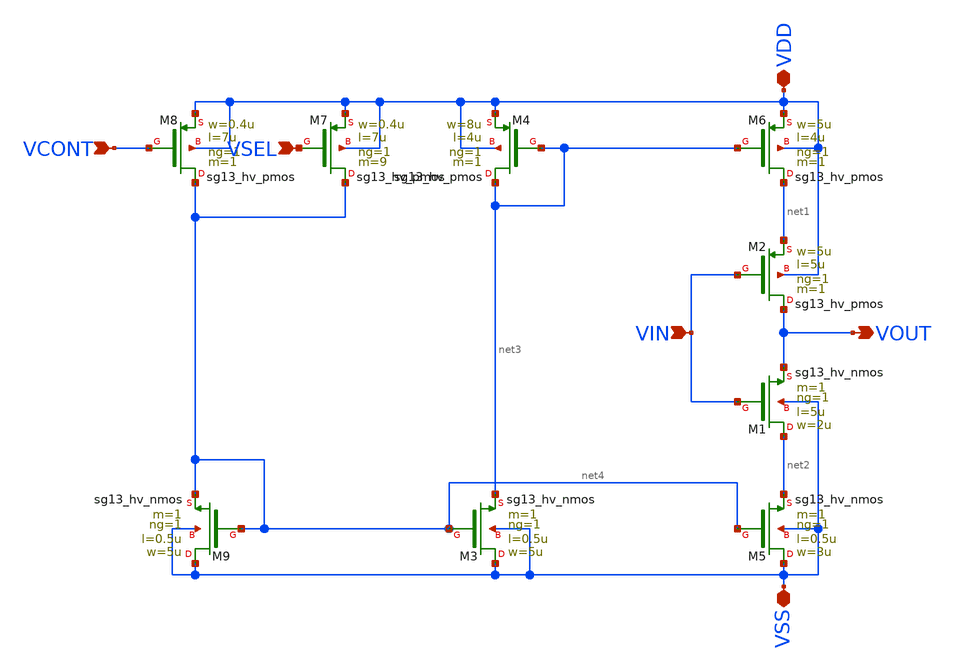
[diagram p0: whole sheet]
** sch_path: ChipUSM_AnalogTrack24/VCO/stage_vto3p1.sch
**.subckt stage_vto3p1 VIN VOUT VDD VSS VCONT VSEL
*.ipin VIN
*.opin VOUT
*.iopin VDD
*.iopin VSS
*.ipin VCONT
*.ipin VSEL
XM9 VSS net4 net4 VSS sg13_hv_nmos w=5u l=0.5u ng=1 m=1 mm_ok=1
XM3 VSS net4 net3 VSS sg13_hv_nmos w=5u l=0.5u ng=1 m=1 mm_ok=1
XM5 VSS net4 net2 VSS sg13_hv_nmos w=3u l=0.5u ng=1 m=1 mm_ok=1
XM8 net4 VCONT VDD VDD sg13_hv_pmos w=0.4u l=7u ng=1 m=1 mm_ok=1
XM4 net3 net3 VDD VDD sg13_hv_pmos w=8u l=4u ng=1 m=1 mm_ok=1
XM6 net1 net3 VDD VDD sg13_hv_pmos w=5u l=4u ng=1 m=1 mm_ok=1
XM2 VOUT VIN net1 VDD sg13_hv_pmos w=5u l=5u ng=1 m=1 mm_ok=1
XM1 net2 VIN VOUT VSS sg13_hv_nmos w=2u l=5u ng=1 m=1 mm_ok=1
XM7 net4 VSEL VDD VDD sg13_hv_pmos w=0.4u l=7u ng=1 m=9 mm_ok=1
**.ends
.end
